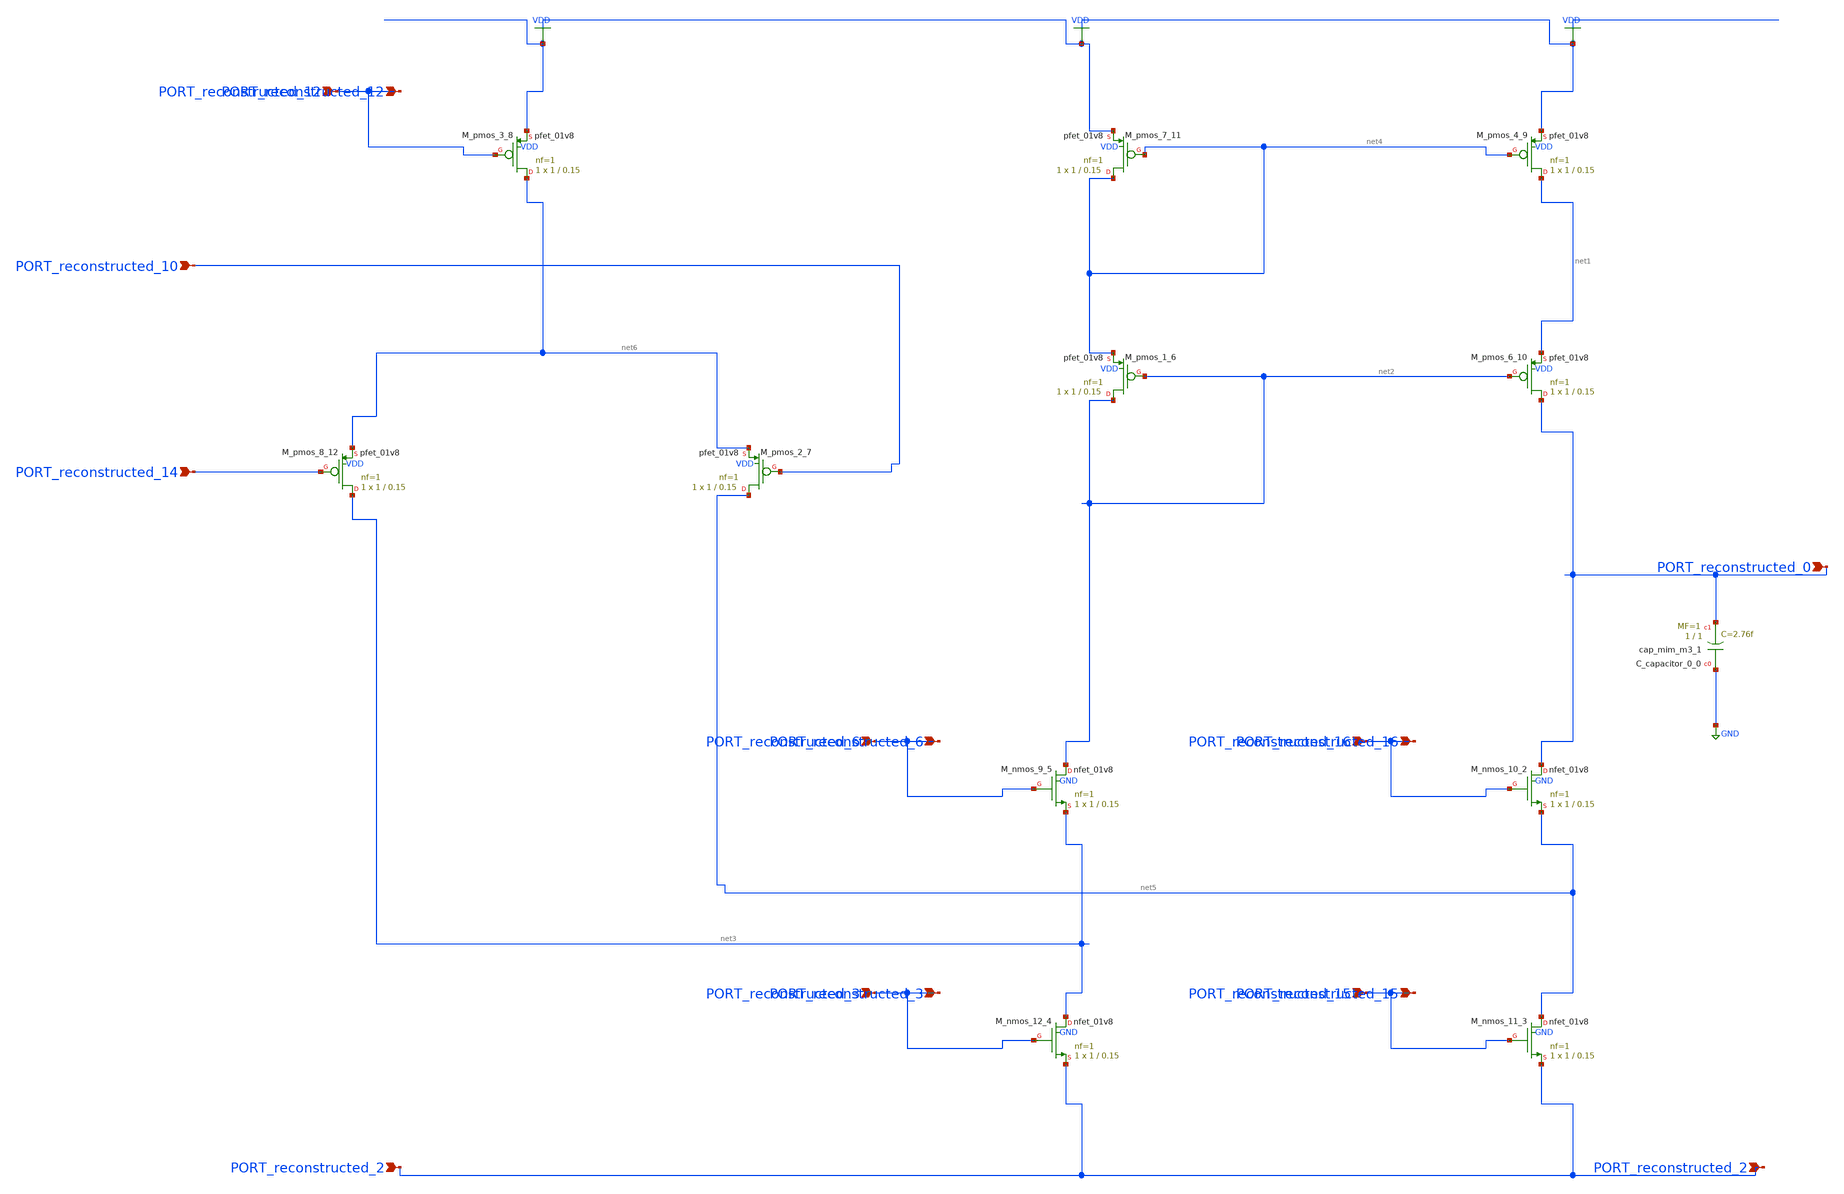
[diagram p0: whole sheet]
** sch_path: schematics/Image2Net/089.sch
**.subckt 089 PORT_reconstructed_14 PORT_reconstructed_10 PORT_reconstructed_3 PORT_reconstructed_15
*+ PORT_reconstructed_6 PORT_reconstructed_16 PORT_reconstructed_0 PORT_reconstructed_2 PORT_reconstructed_6
*+ PORT_reconstructed_12 PORT_reconstructed_15 PORT_reconstructed_16 PORT_reconstructed_12 PORT_reconstructed_3
*+ PORT_reconstructed_2
*.ipin PORT_reconstructed_14
*.ipin PORT_reconstructed_10
*.ipin PORT_reconstructed_3
*.ipin PORT_reconstructed_15
*.ipin PORT_reconstructed_6
*.ipin PORT_reconstructed_16
*.ipin PORT_reconstructed_0
*.ipin PORT_reconstructed_2
*.ipin PORT_reconstructed_6
*.ipin PORT_reconstructed_12
*.ipin PORT_reconstructed_15
*.ipin PORT_reconstructed_16
*.ipin PORT_reconstructed_12
*.ipin PORT_reconstructed_3
*.ipin PORT_reconstructed_2
XC_capacitor_0_0 GND PORT_reconstructed_0 sky130_fd_pr__cap_mim_m3_1 W=1 L=1 MF=1 m=1
XM_nmos_10_2 PORT_reconstructed_0 PORT_reconstructed_16 net5 GND sky130_fd_pr__nfet_01v8 L=0.15 W=1 nf=1
+ ad='int((1 + 1)/2) * 1 / 1 * 0.29' as='int((1 + 2)/2) * 1 / 1 * 0.29' pd='2*int((1 + 1)/2) * (1 / 1 + 0.29)'
+ ps='2*int((1 + 2)/2) * (1 / 1 + 0.29)' nrd='0.29 / 1 ' nrs='0.29 / 1 ' sa=0 sb=0 sd=0 mult=1 m=1
XM_nmos_11_3 net5 PORT_reconstructed_15 PORT_reconstructed_2 GND sky130_fd_pr__nfet_01v8 L=0.15 W=1 nf=1
+ ad='int((1 + 1)/2) * 1 / 1 * 0.29' as='int((1 + 2)/2) * 1 / 1 * 0.29' pd='2*int((1 + 1)/2) * (1 / 1 + 0.29)'
+ ps='2*int((1 + 2)/2) * (1 / 1 + 0.29)' nrd='0.29 / 1 ' nrs='0.29 / 1 ' sa=0 sb=0 sd=0 mult=1 m=1
XM_nmos_12_4 net3 PORT_reconstructed_3 PORT_reconstructed_2 GND sky130_fd_pr__nfet_01v8 L=0.15 W=1 nf=1
+ ad='int((1 + 1)/2) * 1 / 1 * 0.29' as='int((1 + 2)/2) * 1 / 1 * 0.29' pd='2*int((1 + 1)/2) * (1 / 1 + 0.29)'
+ ps='2*int((1 + 2)/2) * (1 / 1 + 0.29)' nrd='0.29 / 1 ' nrs='0.29 / 1 ' sa=0 sb=0 sd=0 mult=1 m=1
XM_nmos_9_5 net2 PORT_reconstructed_6 net3 GND sky130_fd_pr__nfet_01v8 L=0.15 W=1 nf=1 ad='int((1 + 1)/2) * 1 / 1 * 0.29'
+ as='int((1 + 2)/2) * 1 / 1 * 0.29' pd='2*int((1 + 1)/2) * (1 / 1 + 0.29)' ps='2*int((1 + 2)/2) * (1 / 1 + 0.29)'
+ nrd='0.29 / 1 ' nrs='0.29 / 1 ' sa=0 sb=0 sd=0 mult=1 m=1
XM_pmos_1_6 net2 net2 net4 VDD sky130_fd_pr__pfet_01v8 L=0.15 W=1 nf=1 ad='int((1 + 1)/2) * 1 / 1 * 0.29'
+ as='int((1 + 2)/2) * 1 / 1 * 0.29' pd='2*int((1 + 1)/2) * (1 / 1 + 0.29)' ps='2*int((1 + 2)/2) * (1 / 1 + 0.29)'
+ nrd='0.29 / 1 ' nrs='0.29 / 1 ' sa=0 sb=0 sd=0 mult=1 m=1
XM_pmos_2_7 net5 PORT_reconstructed_10 net6 VDD sky130_fd_pr__pfet_01v8 L=0.15 W=1 nf=1 ad='int((1 + 1)/2) * 1 / 1 * 0.29'
+ as='int((1 + 2)/2) * 1 / 1 * 0.29' pd='2*int((1 + 1)/2) * (1 / 1 + 0.29)' ps='2*int((1 + 2)/2) * (1 / 1 + 0.29)'
+ nrd='0.29 / 1 ' nrs='0.29 / 1 ' sa=0 sb=0 sd=0 mult=1 m=1
XM_pmos_3_8 net6 PORT_reconstructed_12 VDD VDD sky130_fd_pr__pfet_01v8 L=0.15 W=1 nf=1 ad='int((1 + 1)/2) * 1 / 1 * 0.29'
+ as='int((1 + 2)/2) * 1 / 1 * 0.29' pd='2*int((1 + 1)/2) * (1 / 1 + 0.29)' ps='2*int((1 + 2)/2) * (1 / 1 + 0.29)'
+ nrd='0.29 / 1 ' nrs='0.29 / 1 ' sa=0 sb=0 sd=0 mult=1 m=1
XM_pmos_4_9 net1 net4 VDD VDD sky130_fd_pr__pfet_01v8 L=0.15 W=1 nf=1 ad='int((1 + 1)/2) * 1 / 1 * 0.29'
+ as='int((1 + 2)/2) * 1 / 1 * 0.29' pd='2*int((1 + 1)/2) * (1 / 1 + 0.29)' ps='2*int((1 + 2)/2) * (1 / 1 + 0.29)'
+ nrd='0.29 / 1 ' nrs='0.29 / 1 ' sa=0 sb=0 sd=0 mult=1 m=1
XM_pmos_6_10 PORT_reconstructed_0 net2 net1 VDD sky130_fd_pr__pfet_01v8 L=0.15 W=1 nf=1 ad='int((1 + 1)/2) * 1 / 1 * 0.29'
+ as='int((1 + 2)/2) * 1 / 1 * 0.29' pd='2*int((1 + 1)/2) * (1 / 1 + 0.29)' ps='2*int((1 + 2)/2) * (1 / 1 + 0.29)'
+ nrd='0.29 / 1 ' nrs='0.29 / 1 ' sa=0 sb=0 sd=0 mult=1 m=1
XM_pmos_7_11 net4 net4 VDD VDD sky130_fd_pr__pfet_01v8 L=0.15 W=1 nf=1 ad='int((1 + 1)/2) * 1 / 1 * 0.29'
+ as='int((1 + 2)/2) * 1 / 1 * 0.29' pd='2*int((1 + 1)/2) * (1 / 1 + 0.29)' ps='2*int((1 + 2)/2) * (1 / 1 + 0.29)'
+ nrd='0.29 / 1 ' nrs='0.29 / 1 ' sa=0 sb=0 sd=0 mult=1 m=1
XM_pmos_8_12 net3 PORT_reconstructed_14 net6 VDD sky130_fd_pr__pfet_01v8 L=0.15 W=1 nf=1 ad='int((1 + 1)/2) * 1 / 1 * 0.29'
+ as='int((1 + 2)/2) * 1 / 1 * 0.29' pd='2*int((1 + 1)/2) * (1 / 1 + 0.29)' ps='2*int((1 + 2)/2) * (1 / 1 + 0.29)'
+ nrd='0.29 / 1 ' nrs='0.29 / 1 ' sa=0 sb=0 sd=0 mult=1 m=1
**.ends
.GLOBAL GND
.GLOBAL VDD
.end
